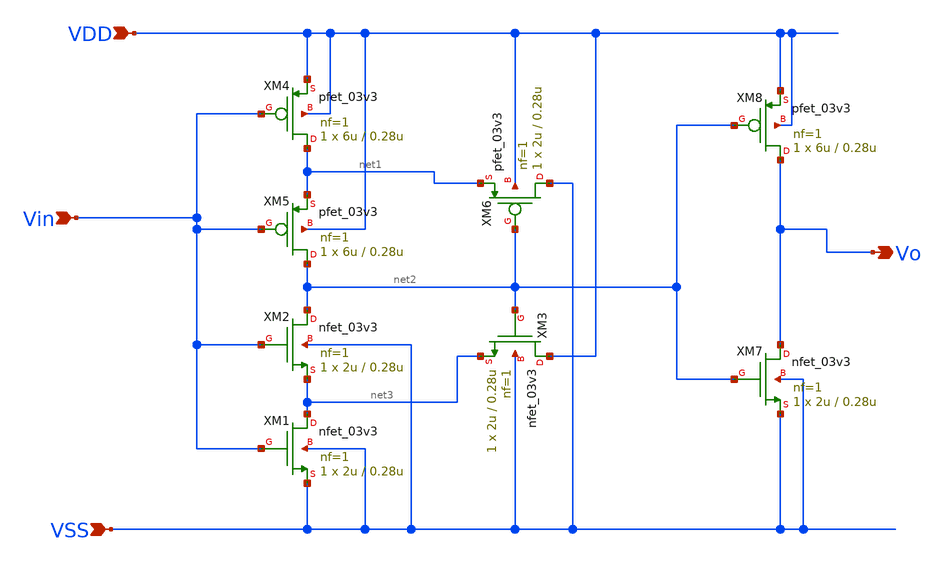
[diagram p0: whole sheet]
** sch_path: designs/switch_matrix_gf180mcu_9t5v0-main/designs/Schmitt.sch
**.subckt Schmitt VDD VSS Vin Vo
*.ipin VDD
*.ipin VSS
*.ipin Vin
*.opin Vo
XM2 net2 Vin net3 VSS nfet_03v3 L=0.28u W=2u nf=1 ad='int((nf+1)/2) * W/nf * 0.18u' as='int((nf+2)/2) * W/nf * 0.18u'
+ pd='2*int((nf+1)/2) * (W/nf + 0.18u)' ps='2*int((nf+2)/2) * (W/nf + 0.18u)' nrd='0.18u / W' nrs='0.18u / W'
+ sa=0 sb=0 sd=0 m=1
XM4 net1 Vin VDD VDD pfet_03v3 L=0.28u W=6u nf=1 ad='int((nf+1)/2) * W/nf * 0.18u' as='int((nf+2)/2) * W/nf * 0.18u'
+ pd='2*int((nf+1)/2) * (W/nf + 0.18u)' ps='2*int((nf+2)/2) * (W/nf + 0.18u)' nrd='0.18u / W' nrs='0.18u / W'
+ sa=0 sb=0 sd=0 m=1
XM5 net2 Vin net1 VDD pfet_03v3 L=0.28u W=6u nf=1 ad='int((nf+1)/2) * W/nf * 0.18u' as='int((nf+2)/2) * W/nf * 0.18u'
+ pd='2*int((nf+1)/2) * (W/nf + 0.18u)' ps='2*int((nf+2)/2) * (W/nf + 0.18u)' nrd='0.18u / W' nrs='0.18u / W'
+ sa=0 sb=0 sd=0 m=1
XM1 net3 Vin VSS VSS nfet_03v3 L=0.28u W=2u nf=1 ad='int((nf+1)/2) * W/nf * 0.18u' as='int((nf+2)/2) * W/nf * 0.18u'
+ pd='2*int((nf+1)/2) * (W/nf + 0.18u)' ps='2*int((nf+2)/2) * (W/nf + 0.18u)' nrd='0.18u / W' nrs='0.18u / W'
+ sa=0 sb=0 sd=0 m=1
XM3 VDD net2 net3 VSS nfet_03v3 L=0.28u W=2u nf=1 ad='int((nf+1)/2) * W/nf * 0.18u' as='int((nf+2)/2) * W/nf * 0.18u'
+ pd='2*int((nf+1)/2) * (W/nf + 0.18u)' ps='2*int((nf+2)/2) * (W/nf + 0.18u)' nrd='0.18u / W' nrs='0.18u / W'
+ sa=0 sb=0 sd=0 m=1
XM6 VSS net2 net1 VDD pfet_03v3 L=0.28u W=2u nf=1 ad='int((nf+1)/2) * W/nf * 0.18u' as='int((nf+2)/2) * W/nf * 0.18u'
+ pd='2*int((nf+1)/2) * (W/nf + 0.18u)' ps='2*int((nf+2)/2) * (W/nf + 0.18u)' nrd='0.18u / W' nrs='0.18u / W'
+ sa=0 sb=0 sd=0 m=1
XM7 Vo net2 VSS VSS nfet_03v3 L=0.28u W=2u nf=1 ad='int((nf+1)/2) * W/nf * 0.18u' as='int((nf+2)/2) * W/nf * 0.18u'
+ pd='2*int((nf+1)/2) * (W/nf + 0.18u)' ps='2*int((nf+2)/2) * (W/nf + 0.18u)' nrd='0.18u / W' nrs='0.18u / W'
+ sa=0 sb=0 sd=0 m=1
XM8 Vo net2 VDD VDD pfet_03v3 L=0.28u W=6u nf=1 ad='int((nf+1)/2) * W/nf * 0.18u' as='int((nf+2)/2) * W/nf * 0.18u'
+ pd='2*int((nf+1)/2) * (W/nf + 0.18u)' ps='2*int((nf+2)/2) * (W/nf + 0.18u)' nrd='0.18u / W' nrs='0.18u / W'
+ sa=0 sb=0 sd=0 m=1
**.ends
.end
